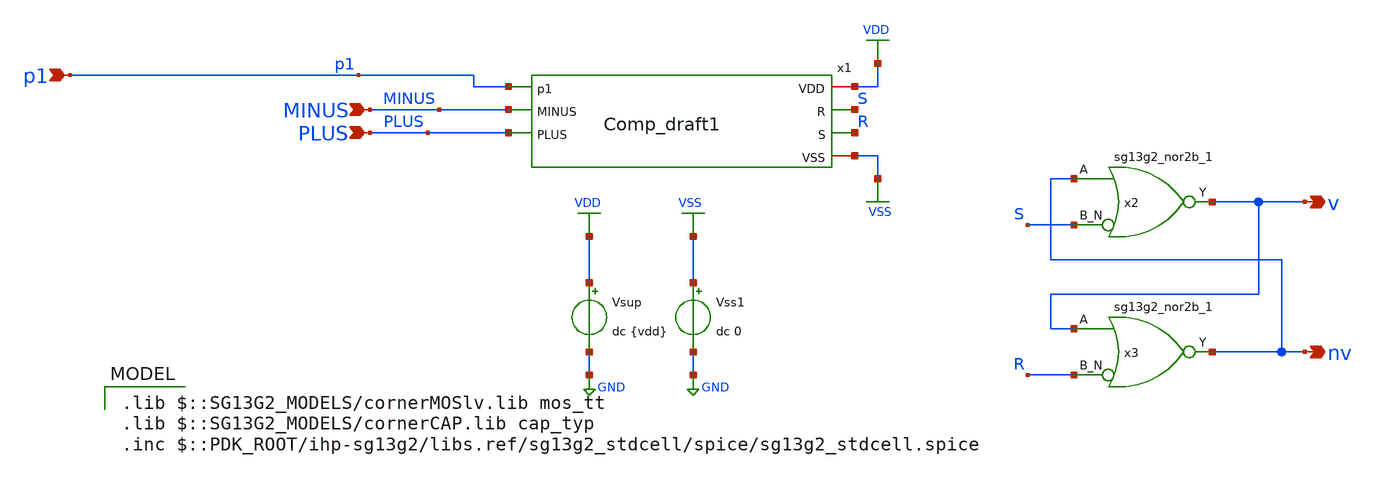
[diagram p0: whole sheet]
** sch_path: DSM/Schematics/Comparator_design_Sneha/COMPARATOR_FINAL/Comp_Latch.sch
**.subckt Comp_Latch v nv PLUS p1 MINUS
*.opin v
*.opin nv
*.ipin PLUS
*.ipin p1
*.ipin MINUS
x2 v nv S VDD VSS sg13g2_nor2b_1
x3 nv v R VDD VSS sg13g2_nor2b_1
x1 VDD p1 S R MINUS PLUS VSS Comp_draft1
Vsup VDD GND dc {vdd}
Vss1 VSS GND dc 0
**** begin user architecture code
 .lib $::SG13G2_MODELS/cornerMOSlv.lib mos_tt
.lib $::SG13G2_MODELS/cornerCAP.lib cap_typ
.inc $::PDK_ROOT/ihp-sg13g2/libs.ref/sg13g2_stdcell/spice/sg13g2_stdcell.spice

**** end user architecture code
**.ends

* expanding   symbol:  sg13g2_stdcells/sg13g2_nor2b_1.sym # of pins=3
** sym_path: sg13g2_stdcells/sg13g2_nor2b_1.sym
** sch_path: sg13g2_stdcells/sg13g2_nor2b_1.sch
.subckt sg13g2_nor2b_1 Y A B_N VDD VSS
*.opin Y
*.ipin B_N
*.ipin A
*.iopin VDD
*.iopin VSS
XM1 B B_N VSS VSS sg13_lv_nmos w=550.00n l=130.00n ng=1 m=1 mm_ok=1
XM2 Y A VSS VSS sg13_lv_nmos w=740.00n l=130.00n ng=1 m=1 mm_ok=1
XM3 Y B VSS VSS sg13_lv_nmos w=740.00n l=130.00n ng=1 m=1 mm_ok=1
XM4 B B_N VDD VDD sg13_lv_pmos w=840.00n l=130.00n ng=1 m=1 mm_ok=1
XM5 net1 B VDD VDD sg13_lv_pmos w=1.12u l=130.00n ng=1 m=1 mm_ok=1
XM6 Y A net1 VDD sg13_lv_pmos w=1.12u l=130.00n ng=1 m=1 mm_ok=1
.ends


* expanding   symbol:
*+  /foss/designs/CEMS_DSM/DSM/Schematics/Comparator_design_Sneha/COMPARATOR_FINAL/Comp_draft1.sym # of pins=7
** sym_path: DSM/Schematics/Comparator_design_Sneha/COMPARATOR_FINAL/Comp_draft1.sym
** sch_path: DSM/Schematics/Comparator_design_Sneha/COMPARATOR_FINAL/Comp_draft1.sch
.subckt Comp_draft1 VDD p1 R S MINUS PLUS VSS
*.ipin PLUS
*.ipin MINUS
*.ipin p1
*.iopin VDD
*.iopin VSS
*.opin R
*.opin S
XMN5 S R net3 VSS sg13_lv_nmos w=1u l=0.18u ng=1 m=1 mm_ok=1
XMP7 net3 p1 VDD VDD sg13_lv_pmos w=0.5u l=0.18u ng=1 m=1 mm_ok=1
XMP8 S p1 VDD VDD sg13_lv_pmos w=0.5u l=0.18u ng=1 m=1 mm_ok=1
XMP9 S R VDD VDD sg13_lv_pmos w=2u l=0.18u ng=1 m=1 mm_ok=1
XMP10 R S VDD VDD sg13_lv_pmos w=2u l=0.18u ng=1 m=1 mm_ok=1
XMP11 R p1 VDD VDD sg13_lv_pmos w=0.5u l=0.18u ng=1 m=1 mm_ok=1
XMP12 net2 p1 VDD VDD sg13_lv_pmos w=0.5u l=0.15u ng=1 m=1 mm_ok=1
XMN6 R S net2 VSS sg13_lv_nmos w=1u l=0.18u ng=1 m=1 mm_ok=1
XMN7 net4 PLUS net1 VSS sg13_lv_nmos w=2u l=0.18u ng=1 m=1 mm_ok=1
XMN8 net2 MINUS net1 VSS sg13_lv_nmos w=2u l=0.18u ng=1 m=1 mm_ok=1
XM7 net1 p1 VSS VSS sg13_lv_nmos w=4u l=0.18u ng=1 m=1 mm_ok=1
.ends

.GLOBAL VDD
.GLOBAL VSS
.GLOBAL GND
.end
